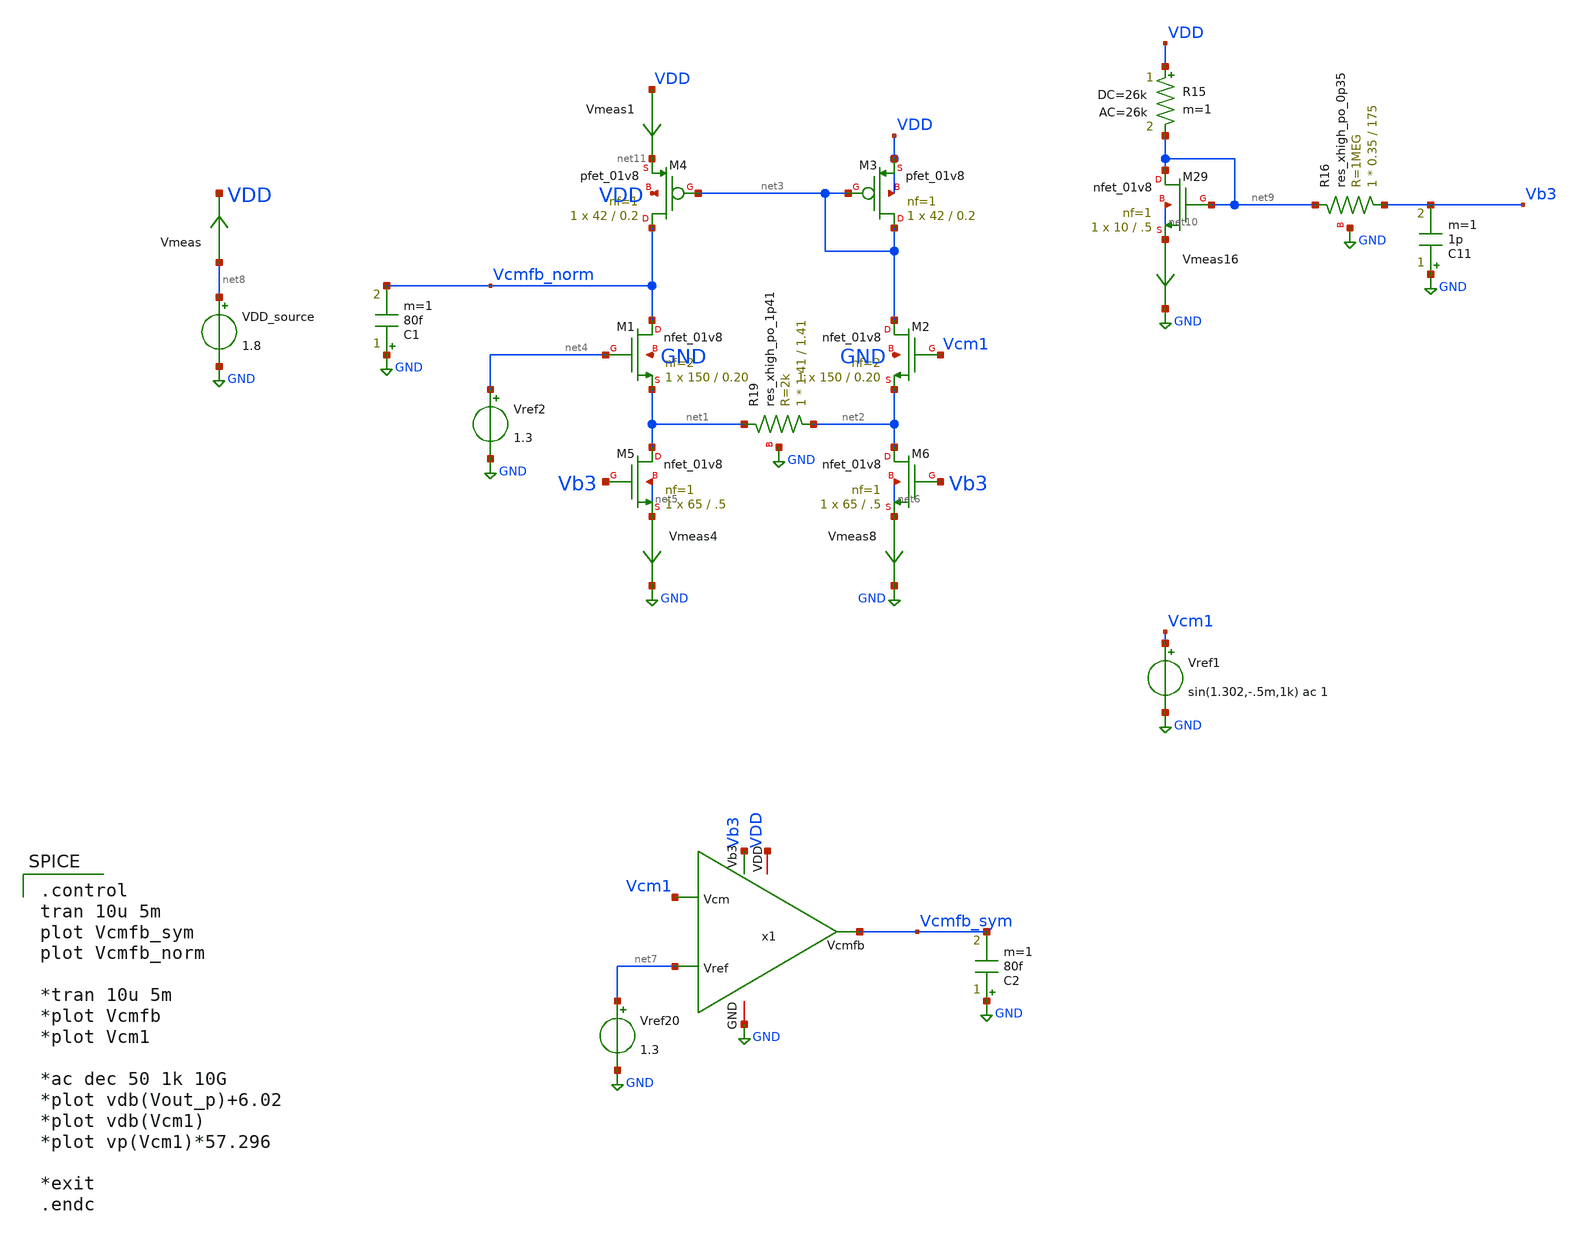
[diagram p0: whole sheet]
** sch_path: schem/cmfb_test.sch
**.subckt cmfb_test
XM1 Vcmfb_norm net4 net1 GND sky130_fd_pr__nfet_01v8 L=0.20 W=150 nf=2 ad='int((nf+1)/2) * W/nf * 0.29'
+ as='int((nf+2)/2) * W/nf * 0.29' pd='2*int((nf+1)/2) * (W/nf + 0.29)' ps='2*int((nf+2)/2) * (W/nf + 0.29)'
+ nrd='0.29 / W' nrs='0.29 / W' sa=0 sb=0 sd=0 mult=1 m=1
XM2 net3 Vcm1 net2 GND sky130_fd_pr__nfet_01v8 L=0.20 W=150 nf=2 ad='int((nf+1)/2) * W/nf * 0.29' as='int((nf+2)/2) * W/nf * 0.29'
+ pd='2*int((nf+1)/2) * (W/nf + 0.29)' ps='2*int((nf+2)/2) * (W/nf + 0.29)' nrd='0.29 / W' nrs='0.29 / W'
+ sa=0 sb=0 sd=0 mult=1 m=1
XM3 net3 net3 VDD VDD sky130_fd_pr__pfet_01v8 L=0.2 W=42 nf=1 ad='int((nf+1)/2) * W/nf * 0.29' as='int((nf+2)/2) * W/nf * 0.29'
+ pd='2*int((nf+1)/2) * (W/nf + 0.29)' ps='2*int((nf+2)/2) * (W/nf + 0.29)' nrd='0.29 / W' nrs='0.29 / W'
+ sa=0 sb=0 sd=0 mult=1 m=1
XM4 Vcmfb_norm net3 net11 VDD sky130_fd_pr__pfet_01v8 L=0.2 W=42 nf=1 ad='int((nf+1)/2) * W/nf * 0.29'
+ as='int((nf+2)/2) * W/nf * 0.29' pd='2*int((nf+1)/2) * (W/nf + 0.29)' ps='2*int((nf+2)/2) * (W/nf + 0.29)'
+ nrd='0.29 / W' nrs='0.29 / W' sa=0 sb=0 sd=0 mult=1 m=1
Vmeas1 VDD net11 0
.save i(vmeas1)
Vref2 net4 GND 1.3
XM5 net1 Vb3 net5 net5 sky130_fd_pr__nfet_01v8 L=.5 W=65 nf=1 ad='int((nf+1)/2) * W/nf * 0.29' as='int((nf+2)/2) * W/nf * 0.29'
+ pd='2*int((nf+1)/2) * (W/nf + 0.29)' ps='2*int((nf+2)/2) * (W/nf + 0.29)' nrd='0.29 / W' nrs='0.29 / W'
+ sa=0 sb=0 sd=0 mult=1 m=1
Vmeas4 net5 GND 0
.save i(vmeas4)
XM6 net2 Vb3 net6 net6 sky130_fd_pr__nfet_01v8 L=.5 W=65 nf=1 ad='int((nf+1)/2) * W/nf * 0.29' as='int((nf+2)/2) * W/nf * 0.29'
+ pd='2*int((nf+1)/2) * (W/nf + 0.29)' ps='2*int((nf+2)/2) * (W/nf + 0.29)' nrd='0.29 / W' nrs='0.29 / W'
+ sa=0 sb=0 sd=0 mult=1 m=1
Vmeas8 net6 GND 0
.save i(vmeas8)
XR19 net2 net1 GND sky130_fd_pr__res_xhigh_po_1p41 L=1.41 mult=1 m=1
Vref20 net7 GND 1.3
x1 Vcm1 net7 Vb3 VDD GND Vcmfb_sym cmfb
VDD_source net8 GND 1.8
Vmeas net8 VDD 0
.save i(vmeas)
XM29 net9 net9 net10 net10 sky130_fd_pr__nfet_01v8 L=.5 W=10 nf=1 ad='int((nf+1)/2) * W/nf * 0.29' as='int((nf+2)/2) * W/nf * 0.29'
+ pd='2*int((nf+1)/2) * (W/nf + 0.29)' ps='2*int((nf+2)/2) * (W/nf + 0.29)' nrd='0.29 / W' nrs='0.29 / W'
+ sa=0 sb=0 sd=0 mult=1 m=1
Vmeas16 net10 GND 0
.save i(vmeas16)
R15 VDD net9 26k ac=26k m=1
XR16 Vb3 net9 GND sky130_fd_pr__res_xhigh_po_0p35 L=175 mult=1 m=1
C11 GND Vb3 1p m=1
Vref1 Vcm1 GND sin(1.302,-.5m,1k) ac 1
C1 GND Vcmfb_norm 80f m=1
C2 GND Vcmfb_sym 80f m=1
**** begin user architecture code

.include $::SKYWATER_MODELS/cells/nfet_01v8/sky130_fd_pr__nfet_01v8__tt.corner.spice
.include $::SKYWATER_MODELS/cells/pfet_01v8/sky130_fd_pr__pfet_01v8__tt.corner.spice
.include $::SKYWATER_MODELS/cells/nfet_01v8_lvt/sky130_fd_pr__nfet_01v8_lvt__tt.corner.spice
*.include $::SKYWATER_MODELS/cells/nfet_03v3_nvt/sky130_fd_pr__nfet_03v3_nvt__tt.corner.spice
*.include $::SKYWATER_MODELS/cells/nfet_05v0_nvt/sky130_fd_pr__nfet_05v0_nvt__tt.corner.spice
*.include $::SKYWATER_MODELS/cells/esd_nfet_01v8/sky130_fd_pr__esd_nfet_01v8__tt.corner.spice
*.include $::SKYWATER_MODELS/cells/pfet_01v8_lvt/sky130_fd_pr__pfet_01v8_lvt__tt.corner.spice
*.include $::SKYWATER_MODELS/cells/pfet_01v8_hvt/sky130_fd_pr__pfet_01v8_hvt__tt.corner.spice
*.include $::SKYWATER_MODELS/models/corners/tt/nonfet.spice
* Mismatch parameters
.include $::SKYWATER_MODELS/cells/nfet_01v8/sky130_fd_pr__nfet_01v8__mismatch.corner.spice
.include $::SKYWATER_MODELS/cells/pfet_01v8/sky130_fd_pr__pfet_01v8__mismatch.corner.spice
.include $::SKYWATER_MODELS/cells/nfet_01v8_lvt/sky130_fd_pr__nfet_01v8_lvt__mismatch.corner.spice
*.include $::SKYWATER_MODELS/cells/pfet_01v8_lvt/sky130_fd_pr__pfet_01v8_lvt__mismatch.corner.spice
*.include $::SKYWATER_MODELS/cells/pfet_01v8_hvt/sky130_fd_pr__pfet_01v8_hvt__mismatch.corner.spice
*.include $::SKYWATER_MODELS/cells/nfet_g5v0d10v5/sky130_fd_pr__nfet_g5v0d10v5__mismatch.corner.spice
*.include $::SKYWATER_MODELS/cells/pfet_g5v0d10v5/sky130_fd_pr__pfet_g5v0d10v5__mismatch.corner.spice
*.include $::SKYWATER_MODELS/cells/nfet_05v0_nvt/sky130_fd_pr__nfet_05v0_nvt__mismatch.corner.spice
*.include $::SKYWATER_MODELS/cells/nfet_03v3_nvt/sky130_fd_pr__nfet_03v3_nvt__mismatch.corner.spice
* Resistor$::SKYWATER_MODELS/Capacitor
.include $::SKYWATER_MODELS/models/r+c/res_typical__cap_typical.spice
.include $::SKYWATER_MODELS/models/r+c/res_typical__cap_typical__lin.spice
* Special cells
*.include $::SKYWATER_MODELS/models/corners/tt/specialized_cells.spice
* All models
.include $::SKYWATER_MODELS/models/all.spice
* Corner
*.include $::SKYWATER_MODELS/models/corners/tt/rf.spice


.option savecurrents
.control
save all
*NFET

save @m.xm90.msky130_fd_pr__nfet_01v8[vds] @m.xm90.msky130_fd_pr__nfet_01v8[gm]
+ @m.xm90.msky130_fd_pr__nfet_01v8[vth] @m.xm90.msky130_fd_pr__nfet_01v8[vgs] @m.xm90.msky130_fd_pr__nfet_01v8[id]
+ @m.xm90.msky130_fd_pr__nfet_01v8[gds] @m.xm90.msky130_fd_pr__nfet_01v8[cgg] @m.xm90.msky130_fd_pr__nfet_01v8[cgs]
+ @m.xm90.msky130_fd_pr__nfet_01v8[cgd] @m.xm90.msky130_fd_pr__nfet_01v8[cgb] @m.xm90.msky130_fd_pr__nfet_01v8[cdg]
+ @m.xm90.msky130_fd_pr__nfet_01v8[cds] @m.xm90.msky130_fd_pr__nfet_01v8[cdd] @m.xm90.msky130_fd_pr__nfet_01v8[cdb]
+ @m.xm90.msky130_fd_pr__nfet_01v8[csg] @m.xm90.msky130_fd_pr__nfet_01v8[css] @m.xm90.msky130_fd_pr__nfet_01v8[csd]
+ @m.xm90.msky130_fd_pr__nfet_01v8[csb] @m.xm90.msky130_fd_pr__nfet_01v8[cbg] @m.xm90.msky130_fd_pr__nfet_01v8[cbs]
+ @m.xm90.msky130_fd_pr__nfet_01v8[cbd] @m.xm90.msky130_fd_pr__nfet_01v8[cbb]
save @m.xm1.msky130_fd_pr__nfet_01v8[vds] @m.xm1.msky130_fd_pr__nfet_01v8[gm]
+ @m.xm1.msky130_fd_pr__nfet_01v8[vth] @m.xm1.msky130_fd_pr__nfet_01v8[vgs] @m.xm1.msky130_fd_pr__nfet_01v8[id]
+ @m.xm1.msky130_fd_pr__nfet_01v8[gds] @m.xm1.msky130_fd_pr__nfet_01v8[cgg] @m.xm1.msky130_fd_pr__nfet_01v8[cgs]
+ @m.xm1.msky130_fd_pr__nfet_01v8[cgd] @m.xm1.msky130_fd_pr__nfet_01v8[cgb] @m.xm1.msky130_fd_pr__nfet_01v8[cdg]
+ @m.xm1.msky130_fd_pr__nfet_01v8[cds] @m.xm1.msky130_fd_pr__nfet_01v8[cdd] @m.xm1.msky130_fd_pr__nfet_01v8[cdb]
+ @m.xm1.msky130_fd_pr__nfet_01v8[csg] @m.xm1.msky130_fd_pr__nfet_01v8[css] @m.xm1.msky130_fd_pr__nfet_01v8[csd]
+ @m.xm1.msky130_fd_pr__nfet_01v8[csb] @m.xm1.msky130_fd_pr__nfet_01v8[cbg] @m.xm1.msky130_fd_pr__nfet_01v8[cbs]
+ @m.xm1.msky130_fd_pr__nfet_01v8[cbd] @m.xm1.msky130_fd_pr__nfet_01v8[cbb]
save @m.xm2.msky130_fd_pr__nfet_01v8[vds] @m.xm2.msky130_fd_pr__nfet_01v8[gm]
+ @m.xm2.msky130_fd_pr__nfet_01v8[vth] @m.xm2.msky130_fd_pr__nfet_01v8[vgs] @m.xm2.msky130_fd_pr__nfet_01v8[id]
+ @m.xm2.msky130_fd_pr__nfet_01v8[gds] @m.xm2.msky130_fd_pr__nfet_01v8[cgg] @m.xm2.msky130_fd_pr__nfet_01v8[cgs]
+ @m.xm2.msky130_fd_pr__nfet_01v8[cgd] @m.xm2.msky130_fd_pr__nfet_01v8[cgb] @m.xm2.msky130_fd_pr__nfet_01v8[cdg]
+ @m.xm2.msky130_fd_pr__nfet_01v8[cds] @m.xm2.msky130_fd_pr__nfet_01v8[cdd] @m.xm2.msky130_fd_pr__nfet_01v8[cdb]
+ @m.xm2.msky130_fd_pr__nfet_01v8[csg] @m.xm2.msky130_fd_pr__nfet_01v8[css] @m.xm2.msky130_fd_pr__nfet_01v8[csd]
+ @m.xm2.msky130_fd_pr__nfet_01v8[csb] @m.xm2.msky130_fd_pr__nfet_01v8[cbg] @m.xm2.msky130_fd_pr__nfet_01v8[cbs]
+ @m.xm2.msky130_fd_pr__nfet_01v8[cbd] @m.xm2.msky130_fd_pr__nfet_01v8[cbb]
save @m.xm3.msky130_fd_pr__nfet_01v8[vds] @m.xm3.msky130_fd_pr__nfet_01v8[gm]
+ @m.xm3.msky130_fd_pr__nfet_01v8[vth] @m.xm3.msky130_fd_pr__nfet_01v8[vgs] @m.xm3.msky130_fd_pr__nfet_01v8[id]
+ @m.xm3.msky130_fd_pr__nfet_01v8[gds] @m.xm3.msky130_fd_pr__nfet_01v8[cgg] @m.xm3.msky130_fd_pr__nfet_01v8[cgs]
+ @m.xm3.msky130_fd_pr__nfet_01v8[cgd] @m.xm3.msky130_fd_pr__nfet_01v8[cgb] @m.xm3.msky130_fd_pr__nfet_01v8[cdg]
+ @m.xm3.msky130_fd_pr__nfet_01v8[cds] @m.xm3.msky130_fd_pr__nfet_01v8[cdd] @m.xm3.msky130_fd_pr__nfet_01v8[cdb]
+ @m.xm3.msky130_fd_pr__nfet_01v8[csg] @m.xm3.msky130_fd_pr__nfet_01v8[css] @m.xm3.msky130_fd_pr__nfet_01v8[csd]
+ @m.xm3.msky130_fd_pr__nfet_01v8[csb] @m.xm3.msky130_fd_pr__nfet_01v8[cbg] @m.xm3.msky130_fd_pr__nfet_01v8[cbs]
+ @m.xm3.msky130_fd_pr__nfet_01v8[cbd] @m.xm3.msky130_fd_pr__nfet_01v8[cbb]
save @m.xm6.msky130_fd_pr__nfet_01v8[vds] @m.xm6.msky130_fd_pr__nfet_01v8[gm]
+ @m.xm6.msky130_fd_pr__nfet_01v8[vth] @m.xm6.msky130_fd_pr__nfet_01v8[vgs] @m.xm6.msky130_fd_pr__nfet_01v8[id]
+ @m.xm6.msky130_fd_pr__nfet_01v8[gds] @m.xm6.msky130_fd_pr__nfet_01v8[cgg] @m.xm6.msky130_fd_pr__nfet_01v8[cgs]
+ @m.xm6.msky130_fd_pr__nfet_01v8[cgd] @m.xm6.msky130_fd_pr__nfet_01v8[cgb] @m.xm6.msky130_fd_pr__nfet_01v8[cdg]
+ @m.xm6.msky130_fd_pr__nfet_01v8[cds] @m.xm6.msky130_fd_pr__nfet_01v8[cdd] @m.xm6.msky130_fd_pr__nfet_01v8[cdb]
+ @m.xm6.msky130_fd_pr__nfet_01v8[csg] @m.xm6.msky130_fd_pr__nfet_01v8[css] @m.xm6.msky130_fd_pr__nfet_01v8[csd]
+ @m.xm6.msky130_fd_pr__nfet_01v8[csb] @m.xm6.msky130_fd_pr__nfet_01v8[cbg] @m.xm6.msky130_fd_pr__nfet_01v8[cbs]
+ @m.xm6.msky130_fd_pr__nfet_01v8[cbd] @m.xm6.msky130_fd_pr__nfet_01v8[cbb]
save @m.xm7.msky130_fd_pr__nfet_01v8[vds] @m.xm7.msky130_fd_pr__nfet_01v8[gm]
+ @m.xm7.msky130_fd_pr__nfet_01v8[vth] @m.xm7.msky130_fd_pr__nfet_01v8[vgs] @m.xm7.msky130_fd_pr__nfet_01v8[id]
+ @m.xm7.msky130_fd_pr__nfet_01v8[gds] @m.xm7.msky130_fd_pr__nfet_01v8[cgg] @m.xm7.msky130_fd_pr__nfet_01v8[cgs]
+ @m.xm7.msky130_fd_pr__nfet_01v8[cgd] @m.xm7.msky130_fd_pr__nfet_01v8[cgb] @m.xm7.msky130_fd_pr__nfet_01v8[cdg]
+ @m.xm7.msky130_fd_pr__nfet_01v8[cds] @m.xm7.msky130_fd_pr__nfet_01v8[cdd] @m.xm7.msky130_fd_pr__nfet_01v8[cdb]
+ @m.xm7.msky130_fd_pr__nfet_01v8[csg] @m.xm7.msky130_fd_pr__nfet_01v8[css] @m.xm7.msky130_fd_pr__nfet_01v8[csd]
+ @m.xm7.msky130_fd_pr__nfet_01v8[csb] @m.xm7.msky130_fd_pr__nfet_01v8[cbg] @m.xm7.msky130_fd_pr__nfet_01v8[cbs]
+ @m.xm7.msky130_fd_pr__nfet_01v8[cbd] @m.xm7.msky130_fd_pr__nfet_01v8[cbb]
save @m.xm8.msky130_fd_pr__nfet_01v8[vds] @m.xm8.msky130_fd_pr__nfet_01v8[gm]
+ @m.xm8.msky130_fd_pr__nfet_01v8[vth] @m.xm8.msky130_fd_pr__nfet_01v8[vgs] @m.xm8.msky130_fd_pr__nfet_01v8[id]
+ @m.xm8.msky130_fd_pr__nfet_01v8[gds] @m.xm8.msky130_fd_pr__nfet_01v8[cgg] @m.xm8.msky130_fd_pr__nfet_01v8[cgs]
+ @m.xm8.msky130_fd_pr__nfet_01v8[cgd] @m.xm8.msky130_fd_pr__nfet_01v8[cgb] @m.xm8.msky130_fd_pr__nfet_01v8[cdg]
+ @m.xm8.msky130_fd_pr__nfet_01v8[cds] @m.xm8.msky130_fd_pr__nfet_01v8[cdd] @m.xm8.msky130_fd_pr__nfet_01v8[cdb]
+ @m.xm8.msky130_fd_pr__nfet_01v8[csg] @m.xm8.msky130_fd_pr__nfet_01v8[css] @m.xm8.msky130_fd_pr__nfet_01v8[csd]
+ @m.xm8.msky130_fd_pr__nfet_01v8[csb] @m.xm8.msky130_fd_pr__nfet_01v8[cbg] @m.xm8.msky130_fd_pr__nfet_01v8[cbs]
+ @m.xm8.msky130_fd_pr__nfet_01v8[cbd] @m.xm8.msky130_fd_pr__nfet_01v8[cbb]
save @m.xm11.msky130_fd_pr__nfet_01v8[vds] @m.xm11.msky130_fd_pr__nfet_01v8[gm]
+ @m.xm11.msky130_fd_pr__nfet_01v8[vth] @m.xm11.msky130_fd_pr__nfet_01v8[vgs] @m.xm11.msky130_fd_pr__nfet_01v8[id]
+ @m.xm11.msky130_fd_pr__nfet_01v8[gds] @m.xm11.msky130_fd_pr__nfet_01v8[cgg] @m.xm11.msky130_fd_pr__nfet_01v8[cgs]
+ @m.xm11.msky130_fd_pr__nfet_01v8[cgd] @m.xm11.msky130_fd_pr__nfet_01v8[cgb] @m.xm11.msky130_fd_pr__nfet_01v8[cdg]
+ @m.xm11.msky130_fd_pr__nfet_01v8[cds] @m.xm11.msky130_fd_pr__nfet_01v8[cdd] @m.xm11.msky130_fd_pr__nfet_01v8[cdb]
+ @m.xm11.msky130_fd_pr__nfet_01v8[csg] @m.xm11.msky130_fd_pr__nfet_01v8[css] @m.xm11.msky130_fd_pr__nfet_01v8[csd]
+ @m.xm11.msky130_fd_pr__nfet_01v8[csb] @m.xm11.msky130_fd_pr__nfet_01v8[cbg] @m.xm11.msky130_fd_pr__nfet_01v8[cbs]
+ @m.xm11.msky130_fd_pr__nfet_01v8[cbd] @m.xm11.msky130_fd_pr__nfet_01v8[cbb]
save @m.xm12.msky130_fd_pr__nfet_01v8[vds] @m.xm12.msky130_fd_pr__nfet_01v8[gm]
+ @m.xm12.msky130_fd_pr__nfet_01v8[vth] @m.xm12.msky130_fd_pr__nfet_01v8[vgs] @m.xm12.msky130_fd_pr__nfet_01v8[id]
+ @m.xm12.msky130_fd_pr__nfet_01v8[gds] @m.xm12.msky130_fd_pr__nfet_01v8[cgg] @m.xm12.msky130_fd_pr__nfet_01v8[cgs]
+ @m.xm12.msky130_fd_pr__nfet_01v8[cgd] @m.xm12.msky130_fd_pr__nfet_01v8[cgb] @m.xm12.msky130_fd_pr__nfet_01v8[cdg]
+ @m.xm12.msky130_fd_pr__nfet_01v8[cds] @m.xm12.msky130_fd_pr__nfet_01v8[cdd] @m.xm12.msky130_fd_pr__nfet_01v8[cdb]
+ @m.xm12.msky130_fd_pr__nfet_01v8[csg] @m.xm12.msky130_fd_pr__nfet_01v8[css] @m.xm12.msky130_fd_pr__nfet_01v8[csd]
+ @m.xm12.msky130_fd_pr__nfet_01v8[csb] @m.xm12.msky130_fd_pr__nfet_01v8[cbg] @m.xm12.msky130_fd_pr__nfet_01v8[cbs]
+ @m.xm12.msky130_fd_pr__nfet_01v8[cbd] @m.xm12.msky130_fd_pr__nfet_01v8[cbb]
save @m.xm16.msky130_fd_pr__nfet_01v8[vds] @m.xm16.msky130_fd_pr__nfet_01v8[gm]
+ @m.xm16.msky130_fd_pr__nfet_01v8[vth] @m.xm16.msky130_fd_pr__nfet_01v8[vgs] @m.xm16.msky130_fd_pr__nfet_01v8[id]
+ @m.xm16.msky130_fd_pr__nfet_01v8[gds] @m.xm16.msky130_fd_pr__nfet_01v8[cgg] @m.xm16.msky130_fd_pr__nfet_01v8[cgs]
+ @m.xm16.msky130_fd_pr__nfet_01v8[cgd] @m.xm16.msky130_fd_pr__nfet_01v8[cgb] @m.xm16.msky130_fd_pr__nfet_01v8[cdg]
+ @m.xm16.msky130_fd_pr__nfet_01v8[cds] @m.xm16.msky130_fd_pr__nfet_01v8[cdd] @m.xm16.msky130_fd_pr__nfet_01v8[cdb]
+ @m.xm16.msky130_fd_pr__nfet_01v8[csg] @m.xm16.msky130_fd_pr__nfet_01v8[css] @m.xm16.msky130_fd_pr__nfet_01v8[csd]
+ @m.xm16.msky130_fd_pr__nfet_01v8[csb] @m.xm16.msky130_fd_pr__nfet_01v8[cbg] @m.xm16.msky130_fd_pr__nfet_01v8[cbs]
+ @m.xm16.msky130_fd_pr__nfet_01v8[cbd] @m.xm16.msky130_fd_pr__nfet_01v8[cbb]
save @m.xm17.msky130_fd_pr__nfet_01v8_lvt[vds] @m.xm17.msky130_fd_pr__nfet_01v8_lvt[gm]
+ @m.xm17.msky130_fd_pr__nfet_01v8_lvt[vth] @m.xm17.msky130_fd_pr__nfet_01v8_lvt[vgs] @m.xm17.msky130_fd_pr__nfet_01v8_lvt[id]
+ @m.xm17.msky130_fd_pr__nfet_01v8_lvt[gds] @m.xm17.msky130_fd_pr__nfet_01v8_lvt[cgg] @m.xm17.msky130_fd_pr__nfet_01v8_lvt[cgs]
+ @m.xm17.msky130_fd_pr__nfet_01v8_lvt[cgd] @m.xm17.msky130_fd_pr__nfet_01v8_lvt[cgb] @m.xm17.msky130_fd_pr__nfet_01v8_lvt[cdg]
+ @m.xm17.msky130_fd_pr__nfet_01v8_lvt[cds] @m.xm17.msky130_fd_pr__nfet_01v8_lvt[cdd] @m.xm17.msky130_fd_pr__nfet_01v8_lvt[cdb]
+ @m.xm17.msky130_fd_pr__nfet_01v8_lvt[csg] @m.xm17.msky130_fd_pr__nfet_01v8_lvt[css] @m.xm17.msky130_fd_pr__nfet_01v8_lvt[csd]
+ @m.xm17.msky130_fd_pr__nfet_01v8_lvt[csb] @m.xm17.msky130_fd_pr__nfet_01v8_lvt[cbg] @m.xm17.msky130_fd_pr__nfet_01v8_lvt[cbs]
+ @m.xm17.msky130_fd_pr__nfet_01v8_lvt[cbd] @m.xm17.msky130_fd_pr__nfet_01v8_lvt[cbb]
save @m.xm18.msky130_fd_pr__nfet_01v8_lvt[vds] @m.xm18.msky130_fd_pr__nfet_01v8_lvt[gm]
+ @m.xm18.msky130_fd_pr__nfet_01v8_lvt[vth] @m.xm18.msky130_fd_pr__nfet_01v8_lvt[vgs] @m.xm18.msky130_fd_pr__nfet_01v8_lvt[id]
+ @m.xm18.msky130_fd_pr__nfet_01v8_lvt[gds] @m.xm18.msky130_fd_pr__nfet_01v8_lvt[cgg] @m.xm18.msky130_fd_pr__nfet_01v8_lvt[cgs]
+ @m.xm18.msky130_fd_pr__nfet_01v8_lvt[cgd] @m.xm18.msky130_fd_pr__nfet_01v8_lvt[cgb] @m.xm18.msky130_fd_pr__nfet_01v8_lvt[cdg]
+ @m.xm18.msky130_fd_pr__nfet_01v8_lvt[cds] @m.xm18.msky130_fd_pr__nfet_01v8_lvt[cdd] @m.xm18.msky130_fd_pr__nfet_01v8_lvt[cdb]
+ @m.xm18.msky130_fd_pr__nfet_01v8_lvt[csg] @m.xm18.msky130_fd_pr__nfet_01v8_lvt[css] @m.xm18.msky130_fd_pr__nfet_01v8_lvt[csd]
+ @m.xm18.msky130_fd_pr__nfet_01v8_lvt[csb] @m.xm18.msky130_fd_pr__nfet_01v8_lvt[cbg] @m.xm18.msky130_fd_pr__nfet_01v8_lvt[cbs]
+ @m.xm18.msky130_fd_pr__nfet_01v8_lvt[cbd] @m.xm18.msky130_fd_pr__nfet_01v8_lvt[cbb]
save @m.xm19.msky130_fd_pr__nfet_01v8[vds] @m.xm19.msky130_fd_pr__nfet_01v8[gm]
+ @m.xm19.msky130_fd_pr__nfet_01v8[vth] @m.xm19.msky130_fd_pr__nfet_01v8[vgs] @m.xm19.msky130_fd_pr__nfet_01v8[id]
+ @m.xm19.msky130_fd_pr__nfet_01v8[gds] @m.xm19.msky130_fd_pr__nfet_01v8[cgg] @m.xm19.msky130_fd_pr__nfet_01v8[cgs]
+ @m.xm19.msky130_fd_pr__nfet_01v8[cgd] @m.xm19.msky130_fd_pr__nfet_01v8[cgb] @m.xm19.msky130_fd_pr__nfet_01v8[cdg]
+ @m.xm19.msky130_fd_pr__nfet_01v8[cds] @m.xm19.msky130_fd_pr__nfet_01v8[cdd] @m.xm19.msky130_fd_pr__nfet_01v8[cdb]
+ @m.xm19.msky130_fd_pr__nfet_01v8[csg] @m.xm19.msky130_fd_pr__nfet_01v8[css] @m.xm19.msky130_fd_pr__nfet_01v8[csd]
+ @m.xm19.msky130_fd_pr__nfet_01v8[csb] @m.xm19.msky130_fd_pr__nfet_01v8[cbg] @m.xm19.msky130_fd_pr__nfet_01v8[cbs]
+ @m.xm19.msky130_fd_pr__nfet_01v8[cbd] @m.xm19.msky130_fd_pr__nfet_01v8[cbb]
save @m.xm30.msky130_fd_pr__nfet_01v8[vds] @m.xm30.msky130_fd_pr__nfet_01v8[gm]
+ @m.xm30.msky130_fd_pr__nfet_01v8[vth] @m.xm30.msky130_fd_pr__nfet_01v8[vgs] @m.xm30.msky130_fd_pr__nfet_01v8[id]
+ @m.xm30.msky130_fd_pr__nfet_01v8[gds] @m.xm30.msky130_fd_pr__nfet_01v8[cgg] @m.xm30.msky130_fd_pr__nfet_01v8[cgs]
+ @m.xm30.msky130_fd_pr__nfet_01v8[cgd] @m.xm30.msky130_fd_pr__nfet_01v8[cgb] @m.xm30.msky130_fd_pr__nfet_01v8[cdg]
+ @m.xm30.msky130_fd_pr__nfet_01v8[cds] @m.xm30.msky130_fd_pr__nfet_01v8[cdd] @m.xm30.msky130_fd_pr__nfet_01v8[cdb]
+ @m.xm30.msky130_fd_pr__nfet_01v8[csg] @m.xm30.msky130_fd_pr__nfet_01v8[css] @m.xm30.msky130_fd_pr__nfet_01v8[csd]
+ @m.xm30.msky130_fd_pr__nfet_01v8[csb] @m.xm30.msky130_fd_pr__nfet_01v8[cbg] @m.xm30.msky130_fd_pr__nfet_01v8[cbs]
+ @m.xm30.msky130_fd_pr__nfet_01v8[cbd] @m.xm30.msky130_fd_pr__nfet_01v8[cbb]
save @m.xm26.msky130_fd_pr__nfet_01v8[vds] @m.xm26.msky130_fd_pr__nfet_01v8[gm]
+ @m.xm26.msky130_fd_pr__nfet_01v8[vth] @m.xm26.msky130_fd_pr__nfet_01v8[vgs] @m.xm26.msky130_fd_pr__nfet_01v8[id]
+ @m.xm26.msky130_fd_pr__nfet_01v8[gds] @m.xm26.msky130_fd_pr__nfet_01v8[cgg] @m.xm26.msky130_fd_pr__nfet_01v8[cgs]
+ @m.xm26.msky130_fd_pr__nfet_01v8[cgd] @m.xm26.msky130_fd_pr__nfet_01v8[cgb] @m.xm26.msky130_fd_pr__nfet_01v8[cdg]
+ @m.xm26.msky130_fd_pr__nfet_01v8[cds] @m.xm26.msky130_fd_pr__nfet_01v8[cdd] @m.xm26.msky130_fd_pr__nfet_01v8[cdb]
+ @m.xm26.msky130_fd_pr__nfet_01v8[csg] @m.xm26.msky130_fd_pr__nfet_01v8[css] @m.xm26.msky130_fd_pr__nfet_01v8[csd]
+ @m.xm26.msky130_fd_pr__nfet_01v8[csb] @m.xm26.msky130_fd_pr__nfet_01v8[cbg] @m.xm26.msky130_fd_pr__nfet_01v8[cbs]
+ @m.xm26.msky130_fd_pr__nfet_01v8[cbd] @m.xm26.msky130_fd_pr__nfet_01v8[cbb]
save @m.xm27.msky130_fd_pr__nfet_01v8[vds] @m.xm27.msky130_fd_pr__nfet_01v8[gm]
+ @m.xm27.msky130_fd_pr__nfet_01v8[vth] @m.xm27.msky130_fd_pr__nfet_01v8[vgs] @m.xm27.msky130_fd_pr__nfet_01v8[id]
+ @m.xm27.msky130_fd_pr__nfet_01v8[gds] @m.xm27.msky130_fd_pr__nfet_01v8[cgg] @m.xm27.msky130_fd_pr__nfet_01v8[cgs]
+ @m.xm27.msky130_fd_pr__nfet_01v8[cgd] @m.xm27.msky130_fd_pr__nfet_01v8[cgb] @m.xm27.msky130_fd_pr__nfet_01v8[cdg]
+ @m.xm27.msky130_fd_pr__nfet_01v8[cds] @m.xm27.msky130_fd_pr__nfet_01v8[cdd] @m.xm27.msky130_fd_pr__nfet_01v8[cdb]
+ @m.xm27.msky130_fd_pr__nfet_01v8[csg] @m.xm27.msky130_fd_pr__nfet_01v8[css] @m.xm27.msky130_fd_pr__nfet_01v8[csd]
+ @m.xm27.msky130_fd_pr__nfet_01v8[csb] @m.xm27.msky130_fd_pr__nfet_01v8[cbg] @m.xm27.msky130_fd_pr__nfet_01v8[cbs]
+ @m.xm27.msky130_fd_pr__nfet_01v8[cbd] @m.xm27.msky130_fd_pr__nfet_01v8[cbb]

*PFET

save @m.xm91.msky130_fd_pr__pfet_01v8[vds] @m.xm91.msky130_fd_pr__pfet_01v8[gm]
+ @m.xm91.msky130_fd_pr__pfet_01v8[vth] @m.xm91.msky130_fd_pr__pfet_01v8[vgs] @m.xm91.msky130_fd_pr__pfet_01v8[id]
+ @m.xm91.msky130_fd_pr__pfet_01v8[gds] @m.xm91.msky130_fd_pr__pfet_01v8[cgg] @m.xm91.msky130_fd_pr__pfet_01v8[cgs]
+ @m.xm91.msky130_fd_pr__pfet_01v8[cgd] @m.xm91.msky130_fd_pr__pfet_01v8[cgb] @m.xm91.msky130_fd_pr__pfet_01v8[cdg]
+ @m.xm91.msky130_fd_pr__pfet_01v8[cds] @m.xm91.msky130_fd_pr__pfet_01v8[cdd] @m.xm91.msky130_fd_pr__pfet_01v8[cdb]
+ @m.xm91.msky130_fd_pr__pfet_01v8[csg] @m.xm91.msky130_fd_pr__pfet_01v8[css] @m.xm91.msky130_fd_pr__pfet_01v8[csd]
+ @m.xm91.msky130_fd_pr__pfet_01v8[csb] @m.xm91.msky130_fd_pr__pfet_01v8[cbg] @m.xm91.msky130_fd_pr__pfet_01v8[cbs]
+ @m.xm91.msky130_fd_pr__pfet_01v8[cbd] @m.xm91.msky130_fd_pr__pfet_01v8[cbb]
save @m.xm4.msky130_fd_pr__pfet_01v8[vds] @m.xm4.msky130_fd_pr__pfet_01v8[gm]
+ @m.xm4.msky130_fd_pr__pfet_01v8[vth] @m.xm4.msky130_fd_pr__pfet_01v8[vgs] @m.xm4.msky130_fd_pr__pfet_01v8[id]
+ @m.xm4.msky130_fd_pr__pfet_01v8[gds] @m.xm4.msky130_fd_pr__pfet_01v8[cgg] @m.xm4.msky130_fd_pr__pfet_01v8[cgs]
+ @m.xm4.msky130_fd_pr__pfet_01v8[cgd] @m.xm4.msky130_fd_pr__pfet_01v8[cgb] @m.xm4.msky130_fd_pr__pfet_01v8[cdg]
+ @m.xm4.msky130_fd_pr__pfet_01v8[cds] @m.xm4.msky130_fd_pr__pfet_01v8[cdd] @m.xm4.msky130_fd_pr__pfet_01v8[cdb]
+ @m.xm4.msky130_fd_pr__pfet_01v8[csg] @m.xm4.msky130_fd_pr__pfet_01v8[css] @m.xm4.msky130_fd_pr__pfet_01v8[csd]
+ @m.xm4.msky130_fd_pr__pfet_01v8[csb] @m.xm4.msky130_fd_pr__pfet_01v8[cbg] @m.xm4.msky130_fd_pr__pfet_01v8[cbs]
+ @m.xm4.msky130_fd_pr__pfet_01v8[cbd] @m.xm4.msky130_fd_pr__pfet_01v8[cbb]
save @m.xm5.msky130_fd_pr__pfet_01v8[vds] @m.xm5.msky130_fd_pr__pfet_01v8[gm]
+ @m.xm5.msky130_fd_pr__pfet_01v8[vth] @m.xm5.msky130_fd_pr__pfet_01v8[vgs] @m.xm5.msky130_fd_pr__pfet_01v8[id]
+ @m.xm5.msky130_fd_pr__pfet_01v8[gds] @m.xm5.msky130_fd_pr__pfet_01v8[cgg] @m.xm5.msky130_fd_pr__pfet_01v8[cgs]
+ @m.xm5.msky130_fd_pr__pfet_01v8[cgd] @m.xm5.msky130_fd_pr__pfet_01v8[cgb] @m.xm5.msky130_fd_pr__pfet_01v8[cdg]
+ @m.xm5.msky130_fd_pr__pfet_01v8[cds] @m.xm5.msky130_fd_pr__pfet_01v8[cdd] @m.xm5.msky130_fd_pr__pfet_01v8[cdb]
+ @m.xm5.msky130_fd_pr__pfet_01v8[csg] @m.xm5.msky130_fd_pr__pfet_01v8[css] @m.xm5.msky130_fd_pr__pfet_01v8[csd]
+ @m.xm5.msky130_fd_pr__pfet_01v8[csb] @m.xm5.msky130_fd_pr__pfet_01v8[cbg] @m.xm5.msky130_fd_pr__pfet_01v8[cbs]
+ @m.xm5.msky130_fd_pr__pfet_01v8[cbd] @m.xm5.msky130_fd_pr__pfet_01v8[cbb]
save @m.xm9.msky130_fd_pr__pfet_01v8[vds] @m.xm9.msky130_fd_pr__pfet_01v8[gm]
+ @m.xm9.msky130_fd_pr__pfet_01v8[vth] @m.xm9.msky130_fd_pr__pfet_01v8[vgs] @m.xm9.msky130_fd_pr__pfet_01v8[id]
+ @m.xm9.msky130_fd_pr__pfet_01v8[gds] @m.xm9.msky130_fd_pr__pfet_01v8[cgg] @m.xm9.msky130_fd_pr__pfet_01v8[cgs]
+ @m.xm9.msky130_fd_pr__pfet_01v8[cgd] @m.xm9.msky130_fd_pr__pfet_01v8[cgb] @m.xm9.msky130_fd_pr__pfet_01v8[cdg]
+ @m.xm9.msky130_fd_pr__pfet_01v8[cds] @m.xm9.msky130_fd_pr__pfet_01v8[cdd] @m.xm9.msky130_fd_pr__pfet_01v8[cdb]
+ @m.xm9.msky130_fd_pr__pfet_01v8[csg] @m.xm9.msky130_fd_pr__pfet_01v8[css] @m.xm9.msky130_fd_pr__pfet_01v8[csd]
+ @m.xm9.msky130_fd_pr__pfet_01v8[csb] @m.xm9.msky130_fd_pr__pfet_01v8[cbg] @m.xm9.msky130_fd_pr__pfet_01v8[cbs]
+ @m.xm9.msky130_fd_pr__pfet_01v8[cbd] @m.xm9.msky130_fd_pr__pfet_01v8[cbb]
save @m.xm10.msky130_fd_pr__pfet_01v8[vds] @m.xm10.msky130_fd_pr__pfet_01v8[gm]
+ @m.xm10.msky130_fd_pr__pfet_01v8[vth] @m.xm10.msky130_fd_pr__pfet_01v8[vgs] @m.xm10.msky130_fd_pr__pfet_01v8[id]
+ @m.xm10.msky130_fd_pr__pfet_01v8[gds] @m.xm10.msky130_fd_pr__pfet_01v8[cgg] @m.xm10.msky130_fd_pr__pfet_01v8[cgs]
+ @m.xm10.msky130_fd_pr__pfet_01v8[cgd] @m.xm10.msky130_fd_pr__pfet_01v8[cgb] @m.xm10.msky130_fd_pr__pfet_01v8[cdg]
+ @m.xm10.msky130_fd_pr__pfet_01v8[cds] @m.xm10.msky130_fd_pr__pfet_01v8[cdd] @m.xm10.msky130_fd_pr__pfet_01v8[cdb]
+ @m.xm10.msky130_fd_pr__pfet_01v8[csg] @m.xm10.msky130_fd_pr__pfet_01v8[css] @m.xm10.msky130_fd_pr__pfet_01v8[csd]
+ @m.xm10.msky130_fd_pr__pfet_01v8[csb] @m.xm10.msky130_fd_pr__pfet_01v8[cbg] @m.xm10.msky130_fd_pr__pfet_01v8[cbs]
+ @m.xm10.msky130_fd_pr__pfet_01v8[cbd] @m.xm10.msky130_fd_pr__pfet_01v8[cbb]
save @m.xm13.msky130_fd_pr__pfet_01v8[vds] @m.xm13.msky130_fd_pr__pfet_01v8[gm]
+ @m.xm13.msky130_fd_pr__pfet_01v8[vth] @m.xm13.msky130_fd_pr__pfet_01v8[vgs] @m.xm13.msky130_fd_pr__pfet_01v8[id]
+ @m.xm13.msky130_fd_pr__pfet_01v8[gds] @m.xm13.msky130_fd_pr__pfet_01v8[cgg] @m.xm13.msky130_fd_pr__pfet_01v8[cgs]
+ @m.xm13.msky130_fd_pr__pfet_01v8[cgd] @m.xm13.msky130_fd_pr__pfet_01v8[cgb] @m.xm13.msky130_fd_pr__pfet_01v8[cdg]
+ @m.xm13.msky130_fd_pr__pfet_01v8[cds] @m.xm13.msky130_fd_pr__pfet_01v8[cdd] @m.xm13.msky130_fd_pr__pfet_01v8[cdb]
+ @m.xm13.msky130_fd_pr__pfet_01v8[csg] @m.xm13.msky130_fd_pr__pfet_01v8[css] @m.xm13.msky130_fd_pr__pfet_01v8[csd]
+ @m.xm13.msky130_fd_pr__pfet_01v8[csb] @m.xm13.msky130_fd_pr__pfet_01v8[cbg] @m.xm13.msky130_fd_pr__pfet_01v8[cbs]
+ @m.xm13.msky130_fd_pr__pfet_01v8[cbd] @m.xm13.msky130_fd_pr__pfet_01v8[cbb]
save @m.xm14.msky130_fd_pr__pfet_01v8[vds] @m.xm14.msky130_fd_pr__pfet_01v8[gm]
+ @m.xm14.msky130_fd_pr__pfet_01v8[vth] @m.xm14.msky130_fd_pr__pfet_01v8[vgs] @m.xm14.msky130_fd_pr__pfet_01v8[id]
+ @m.xm14.msky130_fd_pr__pfet_01v8[gds] @m.xm14.msky130_fd_pr__pfet_01v8[cgg] @m.xm14.msky130_fd_pr__pfet_01v8[cgs]
+ @m.xm14.msky130_fd_pr__pfet_01v8[cgd] @m.xm14.msky130_fd_pr__pfet_01v8[cgb] @m.xm14.msky130_fd_pr__pfet_01v8[cdg]
+ @m.xm14.msky130_fd_pr__pfet_01v8[cds] @m.xm14.msky130_fd_pr__pfet_01v8[cdd] @m.xm14.msky130_fd_pr__pfet_01v8[cdb]
+ @m.xm14.msky130_fd_pr__pfet_01v8[csg] @m.xm14.msky130_fd_pr__pfet_01v8[css] @m.xm14.msky130_fd_pr__pfet_01v8[csd]
+ @m.xm14.msky130_fd_pr__pfet_01v8[csb] @m.xm14.msky130_fd_pr__pfet_01v8[cbg] @m.xm14.msky130_fd_pr__pfet_01v8[cbs]
+ @m.xm14.msky130_fd_pr__pfet_01v8[cbd] @m.xm14.msky130_fd_pr__pfet_01v8[cbb]
save @m.xm24.msky130_fd_pr__pfet_01v8[vds] @m.xm24.msky130_fd_pr__pfet_01v8[gm]
+ @m.xm24.msky130_fd_pr__pfet_01v8[vth] @m.xm24.msky130_fd_pr__pfet_01v8[vgs] @m.xm24.msky130_fd_pr__pfet_01v8[id]
+ @m.xm24.msky130_fd_pr__pfet_01v8[gds] @m.xm24.msky130_fd_pr__pfet_01v8[cgg] @m.xm24.msky130_fd_pr__pfet_01v8[cgs]
+ @m.xm24.msky130_fd_pr__pfet_01v8[cgd] @m.xm24.msky130_fd_pr__pfet_01v8[cgb] @m.xm24.msky130_fd_pr__pfet_01v8[cdg]
+ @m.xm24.msky130_fd_pr__pfet_01v8[cds] @m.xm24.msky130_fd_pr__pfet_01v8[cdd] @m.xm24.msky130_fd_pr__pfet_01v8[cdb]
+ @m.xm24.msky130_fd_pr__pfet_01v8[csg] @m.xm24.msky130_fd_pr__pfet_01v8[css] @m.xm24.msky130_fd_pr__pfet_01v8[csd]
+ @m.xm24.msky130_fd_pr__pfet_01v8[csb] @m.xm24.msky130_fd_pr__pfet_01v8[cbg] @m.xm24.msky130_fd_pr__pfet_01v8[cbs]
+ @m.xm24.msky130_fd_pr__pfet_01v8[cbd] @m.xm24.msky130_fd_pr__pfet_01v8[cbb]
save @m.xm25.msky130_fd_pr__pfet_01v8[vds] @m.xm25.msky130_fd_pr__pfet_01v8[gm]
+ @m.xm25.msky130_fd_pr__pfet_01v8[vth] @m.xm25.msky130_fd_pr__pfet_01v8[vgs] @m.xm25.msky130_fd_pr__pfet_01v8[id]
+ @m.xm25.msky130_fd_pr__pfet_01v8[gds] @m.xm25.msky130_fd_pr__pfet_01v8[cgg] @m.xm25.msky130_fd_pr__pfet_01v8[cgs]
+ @m.xm25.msky130_fd_pr__pfet_01v8[cgd] @m.xm25.msky130_fd_pr__pfet_01v8[cgb] @m.xm25.msky130_fd_pr__pfet_01v8[cdg]
+ @m.xm25.msky130_fd_pr__pfet_01v8[cds] @m.xm25.msky130_fd_pr__pfet_01v8[cdd] @m.xm25.msky130_fd_pr__pfet_01v8[cdb]
+ @m.xm25.msky130_fd_pr__pfet_01v8[csg] @m.xm25.msky130_fd_pr__pfet_01v8[css] @m.xm25.msky130_fd_pr__pfet_01v8[csd]
+ @m.xm25.msky130_fd_pr__pfet_01v8[csb] @m.xm25.msky130_fd_pr__pfet_01v8[cbg] @m.xm25.msky130_fd_pr__pfet_01v8[cbs]
+ @m.xm25.msky130_fd_pr__pfet_01v8[cbd] @m.xm25.msky130_fd_pr__pfet_01v8[cbb]

op
write core_test.raw
.endc


.control
tran 10u 5m
plot Vcmfb_sym
plot Vcmfb_norm

*tran 10u 5m
*plot Vcmfb
*plot Vcm1

*ac dec 50 1k 10G
*plot vdb(Vout_p)+6.02
*plot vdb(Vcm1)
*plot vp(Vcm1)*57.296

*exit
.endc


**** end user architecture code
**.ends

* expanding   symbol:  tia/schem/cmfb.sym # of pins=6
** sym_path: schem/cmfb.sym
** sch_path: schem/cmfb.sch
.subckt cmfb Vcm Vref Vb3 VDD GND Vcmfb
*.iopin VDD
*.iopin GND
*.opin Vcmfb
*.ipin Vref
*.iopin Vb3
*.ipin Vcm
x1 Vref net2 VDD GND Vb3 net3 Vcmfb cmfb_half
x2 Vcm net1 VDD GND Vb3 net3 net3 cmfb_half
XR20 net2 net1 GND sky130_fd_pr__res_xhigh_po W=1.41 L=1.41 mult=1 m=1
.ends


* expanding   symbol:  tia-sscs-pico-2021/schem/cmfb_half.sym # of pins=7
** sym_path: schem/cmfb_half.sym
** sch_path: schem/cmfb_half.sch
.subckt cmfb_half Vin res VDD GND Vb3 diode Vout
*.iopin VDD
*.iopin GND
*.opin Vout
*.ipin Vin
*.iopin diode
*.iopin Vb3
*.iopin res
XM11 Vout Vin res GND sky130_fd_pr__nfet_01v8 L=0.20 W=150 nf=2 ad='int((nf+1)/2) * W/nf * 0.29' as='int((nf+2)/2) * W/nf * 0.29'
+ pd='2*int((nf+1)/2) * (W/nf + 0.29)' ps='2*int((nf+2)/2) * (W/nf + 0.29)' nrd='0.29 / W' nrs='0.29 / W'
+ sa=0 sb=0 sd=0 mult=1 m=1
XM14 Vout diode VDD VDD sky130_fd_pr__pfet_01v8 L=0.2 W=42 nf=1 ad='int((nf+1)/2) * W/nf * 0.29' as='int((nf+2)/2) * W/nf * 0.29'
+ pd='2*int((nf+1)/2) * (W/nf + 0.29)' ps='2*int((nf+2)/2) * (W/nf + 0.29)' nrd='0.29 / W' nrs='0.29 / W'
+ sa=0 sb=0 sd=0 mult=1 m=1
XM15 res Vb3 GND GND sky130_fd_pr__nfet_01v8 L=.5 W=65 nf=1 ad='int((nf+1)/2) * W/nf * 0.29' as='int((nf+2)/2) * W/nf * 0.29'
+ pd='2*int((nf+1)/2) * (W/nf + 0.29)' ps='2*int((nf+2)/2) * (W/nf + 0.29)' nrd='0.29 / W' nrs='0.29 / W'
+ sa=0 sb=0 sd=0 mult=1 m=1
.ends

.GLOBAL GND
.end
